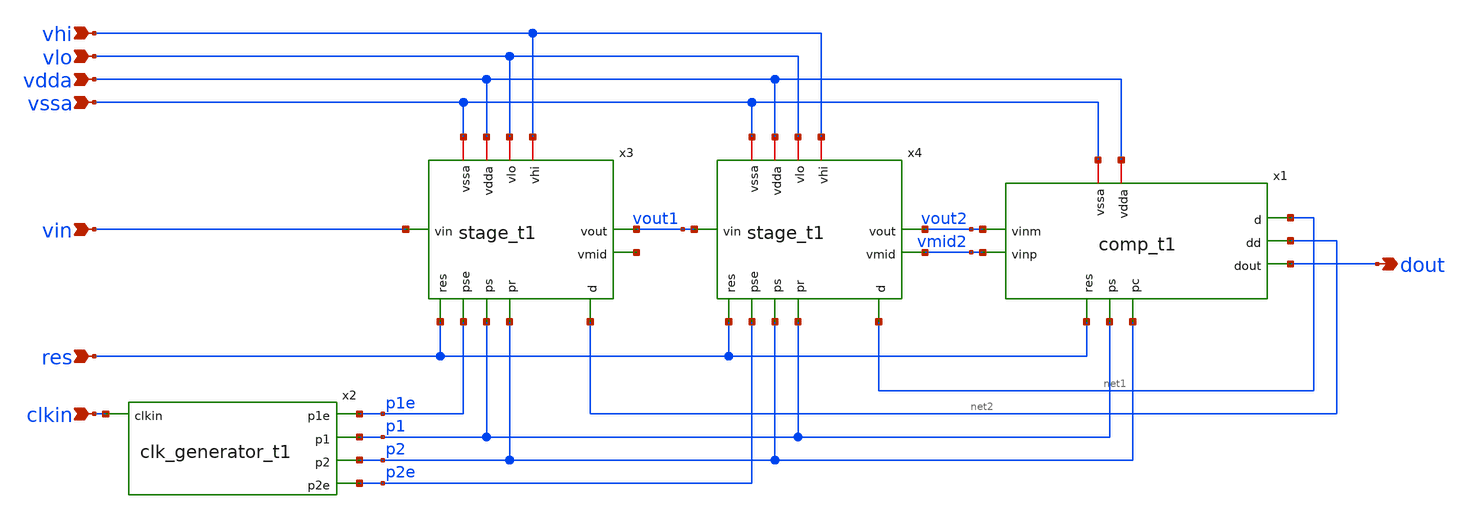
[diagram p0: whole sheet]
** sch_path: 5_Design/4_Layout/Team 1/xschem/IDSM2_t1.sch
**.subckt IDSM2_t1 clkin res vin vssa vdda vlo vhi dout
*.ipin clkin
*.ipin res
*.ipin vin
*.ipin vssa
*.ipin vdda
*.ipin vlo
*.ipin vhi
*.opin dout
x1 vdda p2 net1 net2 vmid2 dout vssa p1 res vout2 comp_t1
x2 p1e clkin p1 p2 p2e clk_generator_t1
x3 res p1e p1 p2 vhi vdda vin vout1 vssa net2 net3 vlo stage_t1
x4 res p2e p2 p1 vhi vdda vout1 vout2 vssa net1 vmid2 vlo stage_t1
**.ends
.end
